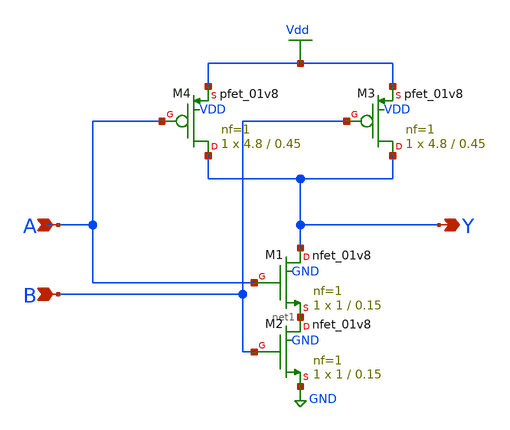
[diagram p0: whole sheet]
** sch_path: Circuiti/logic_gates_sch_sym/nand_2.sch
**.subckt nand_2 A B Y
*.ipin A
*.ipin B
*.opin Y
XM1 Y A net1 GND sky130_fd_pr__nfet_01v8 L=0.15 W=1 nf=1 ad='int((nf+1)/2) * W/nf * 0.29' as='int((nf+2)/2) * W/nf * 0.29'
+ pd='2*int((nf+1)/2) * (W/nf + 0.29)' ps='2*int((nf+2)/2) * (W/nf + 0.29)' nrd='0.29 / W' nrs='0.29 / W'
+ sa=0 sb=0 sd=0 mult=1 m=1
XM3 Y B Vdd VDD sky130_fd_pr__pfet_01v8 L=0.45 W=4.8 nf=1 ad='int((nf+1)/2) * W/nf * 0.29' as='int((nf+2)/2) * W/nf * 0.29'
+ pd='2*int((nf+1)/2) * (W/nf + 0.29)' ps='2*int((nf+2)/2) * (W/nf + 0.29)' nrd='0.29 / W' nrs='0.29 / W'
+ sa=0 sb=0 sd=0 mult=1 m=1
XM4 Y A Vdd VDD sky130_fd_pr__pfet_01v8 L=0.45 W=4.8 nf=1 ad='int((nf+1)/2) * W/nf * 0.29' as='int((nf+2)/2) * W/nf * 0.29'
+ pd='2*int((nf+1)/2) * (W/nf + 0.29)' ps='2*int((nf+2)/2) * (W/nf + 0.29)' nrd='0.29 / W' nrs='0.29 / W'
+ sa=0 sb=0 sd=0 mult=1 m=1
XM2 net1 B GND GND sky130_fd_pr__nfet_01v8 L=0.15 W=1 nf=1 ad='int((nf+1)/2) * W/nf * 0.29' as='int((nf+2)/2) * W/nf * 0.29'
+ pd='2*int((nf+1)/2) * (W/nf + 0.29)' ps='2*int((nf+2)/2) * (W/nf + 0.29)' nrd='0.29 / W' nrs='0.29 / W'
+ sa=0 sb=0 sd=0 mult=1 m=1
**.ends
.GLOBAL Vdd
.GLOBAL GND
.end
